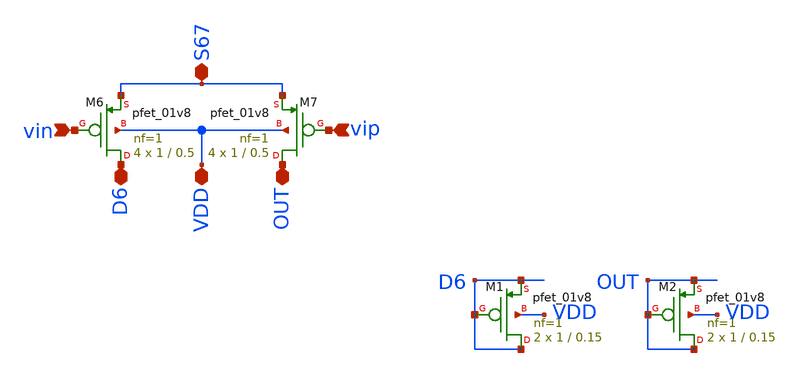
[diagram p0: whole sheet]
** sch_path: OP_Amp/mag/pmosamp.sch
**.subckt pmosamp vip vin D6 OUT VDD S67
*.ipin vip
*.ipin vin
*.iopin D6
*.iopin OUT
*.iopin VDD
*.iopin S67
XM6 D6 vin S67 VDD sky130_fd_pr__pfet_01v8 L=0.5 W=1 nf=1 ad='int((nf+1)/2) * W/nf * 0.29' as='int((nf+2)/2) * W/nf * 0.29'
+ pd='2*int((nf+1)/2) * (W/nf + 0.29)' ps='2*int((nf+2)/2) * (W/nf + 0.29)' nrd='0.29 / W' nrs='0.29 / W'
+ sa=0 sb=0 sd=0 mult=4 m=4
XM7 OUT vip S67 VDD sky130_fd_pr__pfet_01v8 L=0.5 W=1 nf=1 ad='int((nf+1)/2) * W/nf * 0.29' as='int((nf+2)/2) * W/nf * 0.29'
+ pd='2*int((nf+1)/2) * (W/nf + 0.29)' ps='2*int((nf+2)/2) * (W/nf + 0.29)' nrd='0.29 / W' nrs='0.29 / W'
+ sa=0 sb=0 sd=0 mult=4 m=4
XM1 D6 D6 D6 VDD sky130_fd_pr__pfet_01v8 L=0.15 W=1 nf=1 ad='int((nf+1)/2) * W/nf * 0.29' as='int((nf+2)/2) * W/nf * 0.29'
+ pd='2*int((nf+1)/2) * (W/nf + 0.29)' ps='2*int((nf+2)/2) * (W/nf + 0.29)' nrd='0.29 / W' nrs='0.29 / W'
+ sa=0 sb=0 sd=0 mult=2 m=2
XM2 OUT OUT OUT VDD sky130_fd_pr__pfet_01v8 L=0.15 W=1 nf=1 ad='int((nf+1)/2) * W/nf * 0.29' as='int((nf+2)/2) * W/nf * 0.29'
+ pd='2*int((nf+1)/2) * (W/nf + 0.29)' ps='2*int((nf+2)/2) * (W/nf + 0.29)' nrd='0.29 / W' nrs='0.29 / W'
+ sa=0 sb=0 sd=0 mult=2 m=2
**.ends
.end
